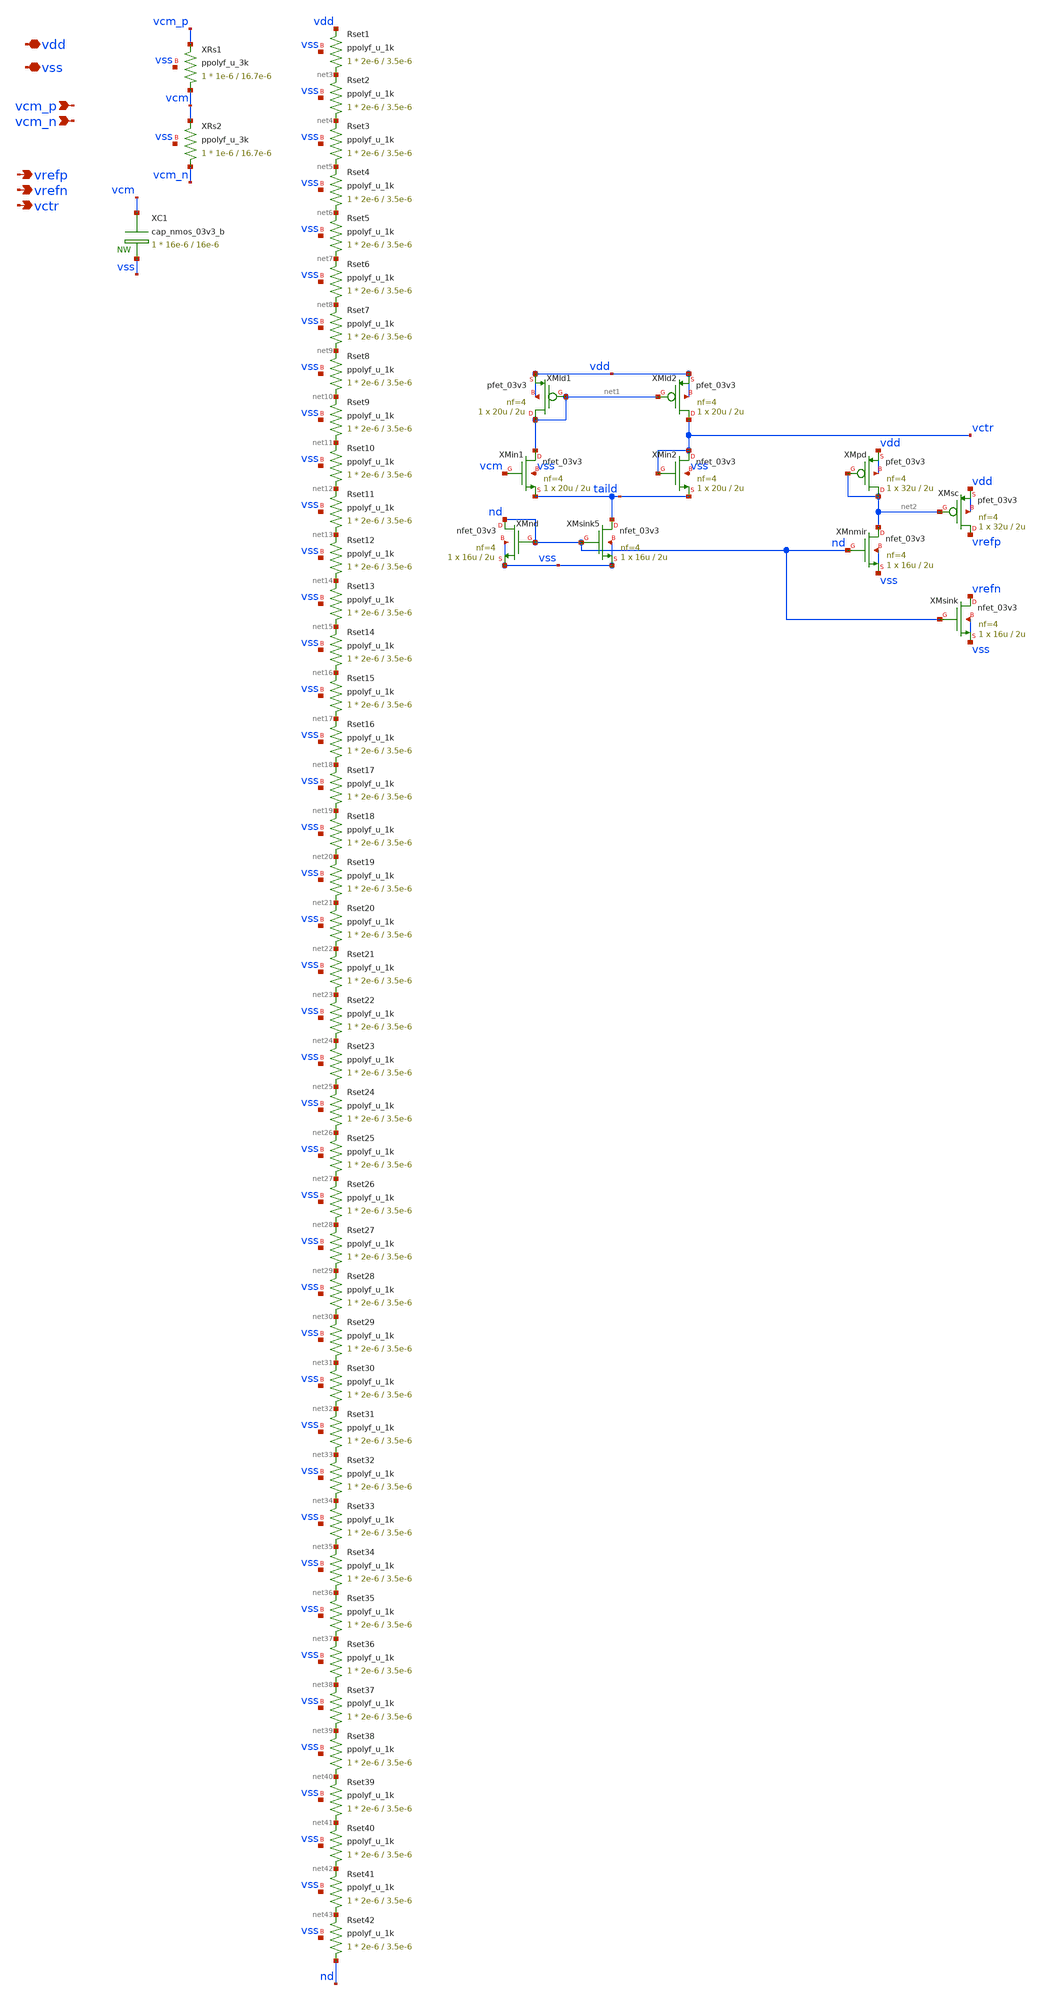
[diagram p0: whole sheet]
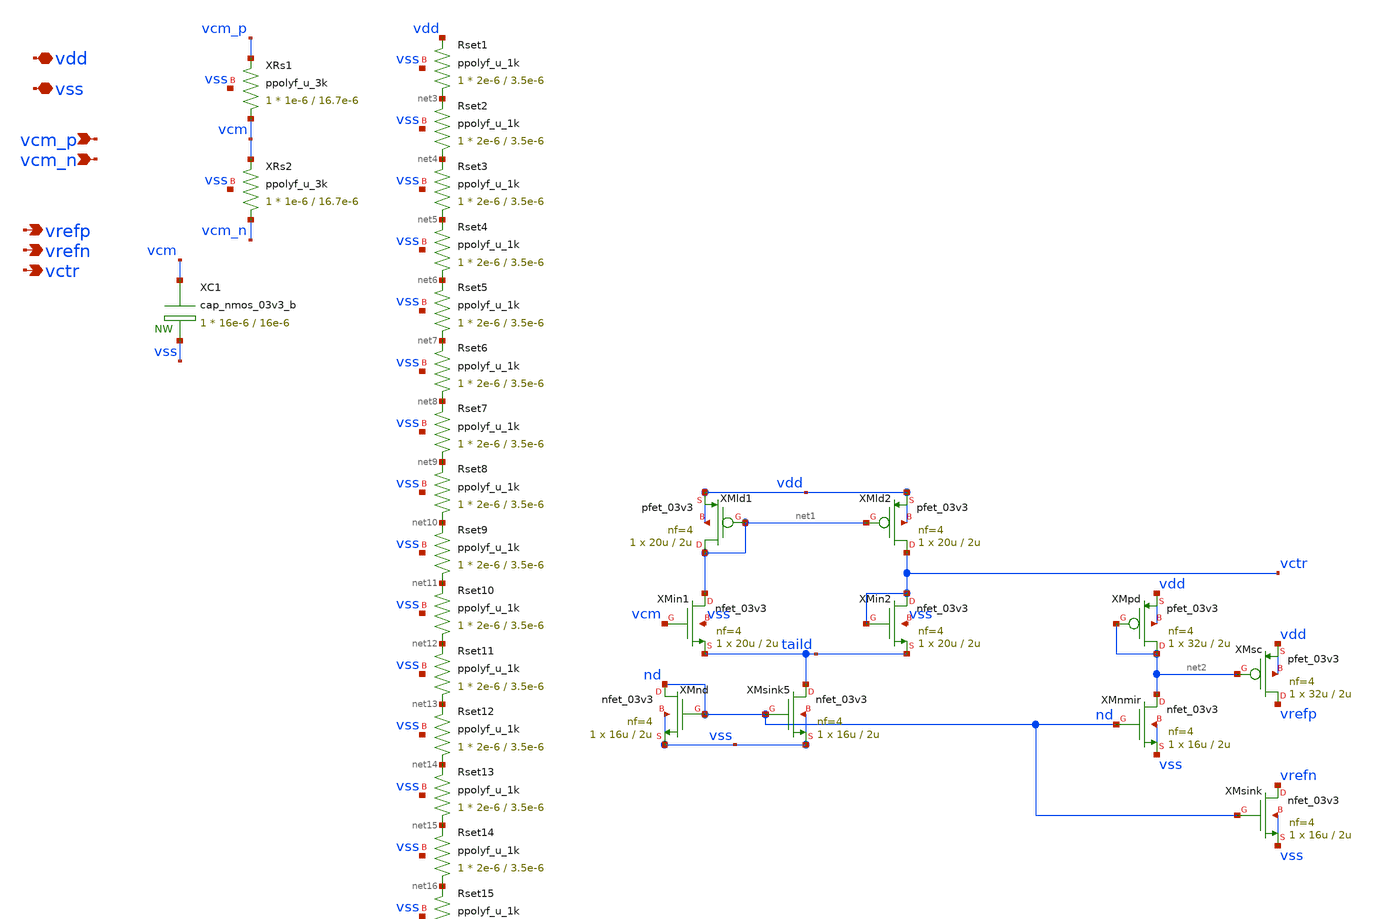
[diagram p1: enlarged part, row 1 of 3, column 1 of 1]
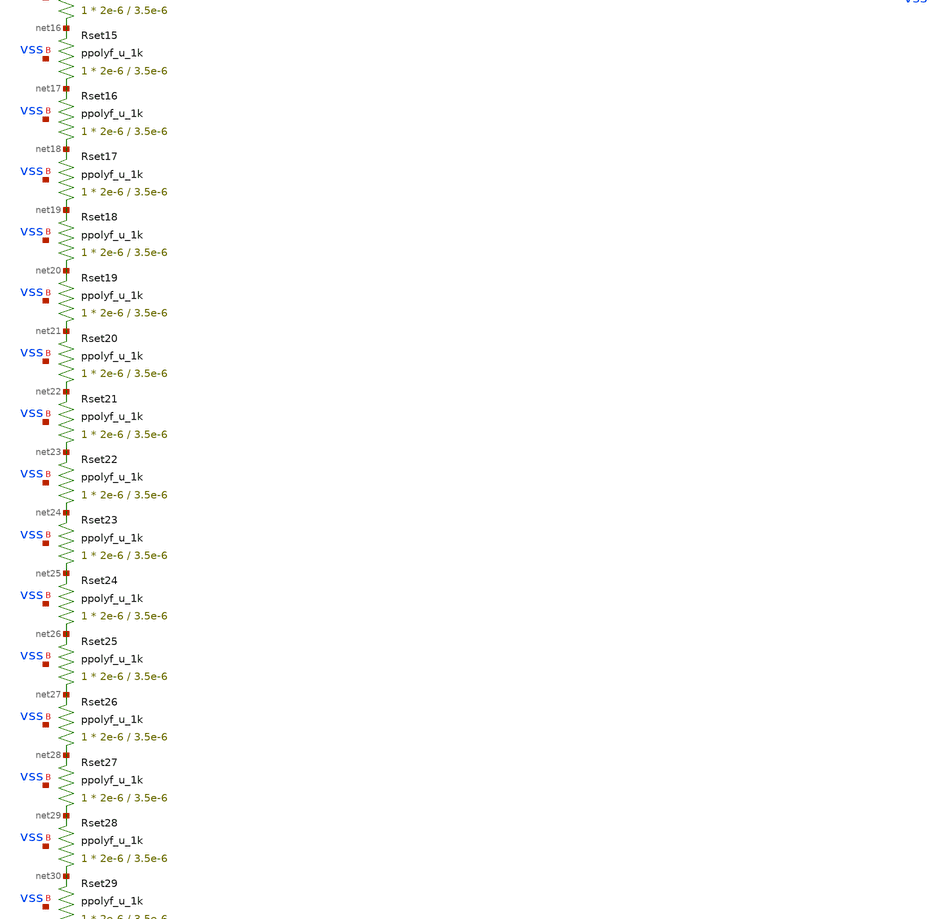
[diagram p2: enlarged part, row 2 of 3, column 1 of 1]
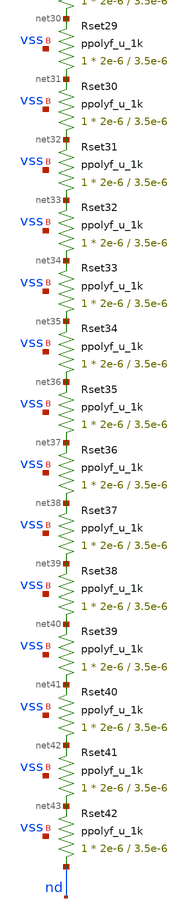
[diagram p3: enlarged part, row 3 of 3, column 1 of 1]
** sch_path: blocks/adc/comp-array/cmref.sch
**.subckt cmref vdd vss vcm_p vcm_n vrefp vrefn vctr
*.iopin vdd
*.iopin vss
*.ipin vcm_p
*.ipin vcm_n
*.opin vrefp
*.opin vrefn
*.opin vctr
XRs1 vcm vcm_p vss ppolyf_u_3k r_width=1e-6 r_length=16.7e-6 m=1
XRs2 vcm_n vcm vss ppolyf_u_3k r_width=1e-6 r_length=16.7e-6 m=1
XRset1 net3 vdd vss ppolyf_u_1k r_width=2e-6 r_length=3.5e-6 m=1
XRset2 net4 net3 vss ppolyf_u_1k r_width=2e-6 r_length=3.5e-6 m=1
XRset3 net5 net4 vss ppolyf_u_1k r_width=2e-6 r_length=3.5e-6 m=1
XRset4 net6 net5 vss ppolyf_u_1k r_width=2e-6 r_length=3.5e-6 m=1
XRset5 net7 net6 vss ppolyf_u_1k r_width=2e-6 r_length=3.5e-6 m=1
XRset6 net8 net7 vss ppolyf_u_1k r_width=2e-6 r_length=3.5e-6 m=1
XRset7 net9 net8 vss ppolyf_u_1k r_width=2e-6 r_length=3.5e-6 m=1
XRset8 net10 net9 vss ppolyf_u_1k r_width=2e-6 r_length=3.5e-6 m=1
XRset9 net11 net10 vss ppolyf_u_1k r_width=2e-6 r_length=3.5e-6 m=1
XRset10 net12 net11 vss ppolyf_u_1k r_width=2e-6 r_length=3.5e-6 m=1
XRset11 net13 net12 vss ppolyf_u_1k r_width=2e-6 r_length=3.5e-6 m=1
XRset12 net14 net13 vss ppolyf_u_1k r_width=2e-6 r_length=3.5e-6 m=1
XRset13 net15 net14 vss ppolyf_u_1k r_width=2e-6 r_length=3.5e-6 m=1
XRset14 net16 net15 vss ppolyf_u_1k r_width=2e-6 r_length=3.5e-6 m=1
XRset15 net17 net16 vss ppolyf_u_1k r_width=2e-6 r_length=3.5e-6 m=1
XRset16 net18 net17 vss ppolyf_u_1k r_width=2e-6 r_length=3.5e-6 m=1
XRset17 net19 net18 vss ppolyf_u_1k r_width=2e-6 r_length=3.5e-6 m=1
XRset18 net20 net19 vss ppolyf_u_1k r_width=2e-6 r_length=3.5e-6 m=1
XRset19 net21 net20 vss ppolyf_u_1k r_width=2e-6 r_length=3.5e-6 m=1
XRset20 net22 net21 vss ppolyf_u_1k r_width=2e-6 r_length=3.5e-6 m=1
XRset21 net23 net22 vss ppolyf_u_1k r_width=2e-6 r_length=3.5e-6 m=1
XRset22 net24 net23 vss ppolyf_u_1k r_width=2e-6 r_length=3.5e-6 m=1
XRset23 net25 net24 vss ppolyf_u_1k r_width=2e-6 r_length=3.5e-6 m=1
XRset24 net26 net25 vss ppolyf_u_1k r_width=2e-6 r_length=3.5e-6 m=1
XRset25 net27 net26 vss ppolyf_u_1k r_width=2e-6 r_length=3.5e-6 m=1
XRset26 net28 net27 vss ppolyf_u_1k r_width=2e-6 r_length=3.5e-6 m=1
XRset27 net29 net28 vss ppolyf_u_1k r_width=2e-6 r_length=3.5e-6 m=1
XRset28 net30 net29 vss ppolyf_u_1k r_width=2e-6 r_length=3.5e-6 m=1
XRset29 net31 net30 vss ppolyf_u_1k r_width=2e-6 r_length=3.5e-6 m=1
XRset30 net32 net31 vss ppolyf_u_1k r_width=2e-6 r_length=3.5e-6 m=1
XRset31 net33 net32 vss ppolyf_u_1k r_width=2e-6 r_length=3.5e-6 m=1
XRset32 net34 net33 vss ppolyf_u_1k r_width=2e-6 r_length=3.5e-6 m=1
XRset33 net35 net34 vss ppolyf_u_1k r_width=2e-6 r_length=3.5e-6 m=1
XRset34 net36 net35 vss ppolyf_u_1k r_width=2e-6 r_length=3.5e-6 m=1
XRset35 net37 net36 vss ppolyf_u_1k r_width=2e-6 r_length=3.5e-6 m=1
XRset36 net38 net37 vss ppolyf_u_1k r_width=2e-6 r_length=3.5e-6 m=1
XRset37 net39 net38 vss ppolyf_u_1k r_width=2e-6 r_length=3.5e-6 m=1
XRset38 net40 net39 vss ppolyf_u_1k r_width=2e-6 r_length=3.5e-6 m=1
XRset39 net41 net40 vss ppolyf_u_1k r_width=2e-6 r_length=3.5e-6 m=1
XRset40 net42 net41 vss ppolyf_u_1k r_width=2e-6 r_length=3.5e-6 m=1
XRset41 net43 net42 vss ppolyf_u_1k r_width=2e-6 r_length=3.5e-6 m=1
XRset42 nd net43 vss ppolyf_u_1k r_width=2e-6 r_length=3.5e-6 m=1
XMnd nd nd vss vss nfet_03v3 L=2u W=16u nf=4 ad='int((nf+1)/2) * W/nf * 0.18u' as='int((nf+2)/2) * W/nf * 0.18u'
+ pd='2*int((nf+1)/2) * (W/nf + 0.18u)' ps='2*int((nf+2)/2) * (W/nf + 0.18u)' nrd='0.18u / W' nrs='0.18u / W'
+ sa=0 sb=0 sd=0 m=1
XMnmir net2 nd vss vss nfet_03v3 L=2u W=16u nf=4 ad='int((nf+1)/2) * W/nf * 0.18u' as='int((nf+2)/2) * W/nf * 0.18u'
+ pd='2*int((nf+1)/2) * (W/nf + 0.18u)' ps='2*int((nf+2)/2) * (W/nf + 0.18u)' nrd='0.18u / W' nrs='0.18u / W'
+ sa=0 sb=0 sd=0 m=1
XMpd net2 net2 vdd vdd pfet_03v3 L=2u W=32u nf=4 ad='int((nf+1)/2) * W/nf * 0.18u' as='int((nf+2)/2) * W/nf * 0.18u'
+ pd='2*int((nf+1)/2) * (W/nf + 0.18u)' ps='2*int((nf+2)/2) * (W/nf + 0.18u)' nrd='0.18u / W' nrs='0.18u / W'
+ sa=0 sb=0 sd=0 m=1
XMsc vrefp net2 vdd vdd pfet_03v3 L=2u W=32u nf=4 ad='int((nf+1)/2) * W/nf * 0.18u' as='int((nf+2)/2) * W/nf * 0.18u'
+ pd='2*int((nf+1)/2) * (W/nf + 0.18u)' ps='2*int((nf+2)/2) * (W/nf + 0.18u)' nrd='0.18u / W' nrs='0.18u / W'
+ sa=0 sb=0 sd=0 m=1
XMsink vrefn nd vss vss nfet_03v3 L=2u W=16u nf=4 ad='int((nf+1)/2) * W/nf * 0.18u' as='int((nf+2)/2) * W/nf * 0.18u'
+ pd='2*int((nf+1)/2) * (W/nf + 0.18u)' ps='2*int((nf+2)/2) * (W/nf + 0.18u)' nrd='0.18u / W' nrs='0.18u / W'
+ sa=0 sb=0 sd=0 m=1
XMsink5 taild nd vss vss nfet_03v3 L=2u W=16u nf=4 ad='int((nf+1)/2) * W/nf * 0.18u' as='int((nf+2)/2) * W/nf * 0.18u'
+ pd='2*int((nf+1)/2) * (W/nf + 0.18u)' ps='2*int((nf+2)/2) * (W/nf + 0.18u)' nrd='0.18u / W' nrs='0.18u / W'
+ sa=0 sb=0 sd=0 m=1
XMin1 net1 vcm taild vss nfet_03v3 L=2u W=20u nf=4 ad='int((nf+1)/2) * W/nf * 0.18u' as='int((nf+2)/2) * W/nf * 0.18u'
+ pd='2*int((nf+1)/2) * (W/nf + 0.18u)' ps='2*int((nf+2)/2) * (W/nf + 0.18u)' nrd='0.18u / W' nrs='0.18u / W'
+ sa=0 sb=0 sd=0 m=1
XMin2 vctr vctr taild vss nfet_03v3 L=2u W=20u nf=4 ad='int((nf+1)/2) * W/nf * 0.18u' as='int((nf+2)/2) * W/nf * 0.18u'
+ pd='2*int((nf+1)/2) * (W/nf + 0.18u)' ps='2*int((nf+2)/2) * (W/nf + 0.18u)' nrd='0.18u / W' nrs='0.18u / W'
+ sa=0 sb=0 sd=0 m=1
XMld2 vctr net1 vdd vdd pfet_03v3 L=2u W=20u nf=4 ad='int((nf+1)/2) * W/nf * 0.18u' as='int((nf+2)/2) * W/nf * 0.18u'
+ pd='2*int((nf+1)/2) * (W/nf + 0.18u)' ps='2*int((nf+2)/2) * (W/nf + 0.18u)' nrd='0.18u / W' nrs='0.18u / W'
+ sa=0 sb=0 sd=0 m=1
XMld1 net1 net1 vdd vdd pfet_03v3 L=2u W=20u nf=4 ad='int((nf+1)/2) * W/nf * 0.18u' as='int((nf+2)/2) * W/nf * 0.18u'
+ pd='2*int((nf+1)/2) * (W/nf + 0.18u)' ps='2*int((nf+2)/2) * (W/nf + 0.18u)' nrd='0.18u / W' nrs='0.18u / W'
+ sa=0 sb=0 sd=0 m=1
XC1 vcm vss cap_nmos_03v3_b c_width=16e-6 c_length=16e-6 m=1
**.ends
.end
